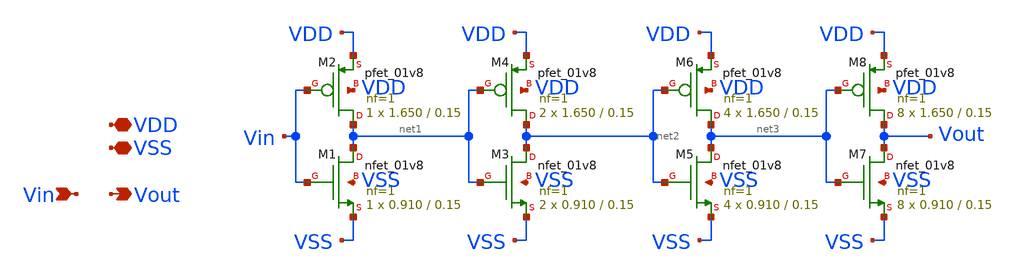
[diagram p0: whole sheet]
** sch_path: xschem/src/capacitor_switch8/capacitor_switch8.sch
**.subckt capacitor_switch8 VDD Vin Vout VSS
*.iopin VDD
*.ipin Vin
*.opin Vout
*.iopin VSS
XM1 net1 Vin VSS VSS sky130_fd_pr__nfet_01v8 L=0.15 W=0.910 nf=1 ad='int((nf+1)/2) * W/nf * 0.29' as='int((nf+2)/2) * W/nf * 0.29'
+ pd='2*int((nf+1)/2) * (W/nf + 0.29)' ps='2*int((nf+2)/2) * (W/nf + 0.29)' nrd='0.29 / W' nrs='0.29 / W'
+ sa=0 sb=0 sd=0 mult=1 m=1
XM2 net1 Vin VDD VDD sky130_fd_pr__pfet_01v8 L=0.15 W=1.650 nf=1 ad='int((nf+1)/2) * W/nf * 0.29' as='int((nf+2)/2) * W/nf * 0.29'
+ pd='2*int((nf+1)/2) * (W/nf + 0.29)' ps='2*int((nf+2)/2) * (W/nf + 0.29)' nrd='0.29 / W' nrs='0.29 / W'
+ sa=0 sb=0 sd=0 mult=1 m=1
XM3 net2 net1 VSS VSS sky130_fd_pr__nfet_01v8 L=0.15 W=0.910 nf=1 ad='int((nf+1)/2) * W/nf * 0.29' as='int((nf+2)/2) * W/nf * 0.29'
+ pd='2*int((nf+1)/2) * (W/nf + 0.29)' ps='2*int((nf+2)/2) * (W/nf + 0.29)' nrd='0.29 / W' nrs='0.29 / W'
+ sa=0 sb=0 sd=0 mult=2 m=2
XM4 net2 net1 VDD VDD sky130_fd_pr__pfet_01v8 L=0.15 W=1.650 nf=1 ad='int((nf+1)/2) * W/nf * 0.29' as='int((nf+2)/2) * W/nf * 0.29'
+ pd='2*int((nf+1)/2) * (W/nf + 0.29)' ps='2*int((nf+2)/2) * (W/nf + 0.29)' nrd='0.29 / W' nrs='0.29 / W'
+ sa=0 sb=0 sd=0 mult=2 m=2
XM5 net3 net2 VSS VSS sky130_fd_pr__nfet_01v8 L=0.15 W=0.910 nf=1 ad='int((nf+1)/2) * W/nf * 0.29' as='int((nf+2)/2) * W/nf * 0.29'
+ pd='2*int((nf+1)/2) * (W/nf + 0.29)' ps='2*int((nf+2)/2) * (W/nf + 0.29)' nrd='0.29 / W' nrs='0.29 / W'
+ sa=0 sb=0 sd=0 mult=4 m=4
XM6 net3 net2 VDD VDD sky130_fd_pr__pfet_01v8 L=0.15 W=1.650 nf=1 ad='int((nf+1)/2) * W/nf * 0.29' as='int((nf+2)/2) * W/nf * 0.29'
+ pd='2*int((nf+1)/2) * (W/nf + 0.29)' ps='2*int((nf+2)/2) * (W/nf + 0.29)' nrd='0.29 / W' nrs='0.29 / W'
+ sa=0 sb=0 sd=0 mult=4 m=4
XM7 Vout net3 VSS VSS sky130_fd_pr__nfet_01v8 L=0.15 W=0.910 nf=1 ad='int((nf+1)/2) * W/nf * 0.29' as='int((nf+2)/2) * W/nf * 0.29'
+ pd='2*int((nf+1)/2) * (W/nf + 0.29)' ps='2*int((nf+2)/2) * (W/nf + 0.29)' nrd='0.29 / W' nrs='0.29 / W'
+ sa=0 sb=0 sd=0 mult=8 m=8
XM8 Vout net3 VDD VDD sky130_fd_pr__pfet_01v8 L=0.15 W=1.650 nf=1 ad='int((nf+1)/2) * W/nf * 0.29' as='int((nf+2)/2) * W/nf * 0.29'
+ pd='2*int((nf+1)/2) * (W/nf + 0.29)' ps='2*int((nf+2)/2) * (W/nf + 0.29)' nrd='0.29 / W' nrs='0.29 / W'
+ sa=0 sb=0 sd=0 mult=8 m=8
**.ends
.end
